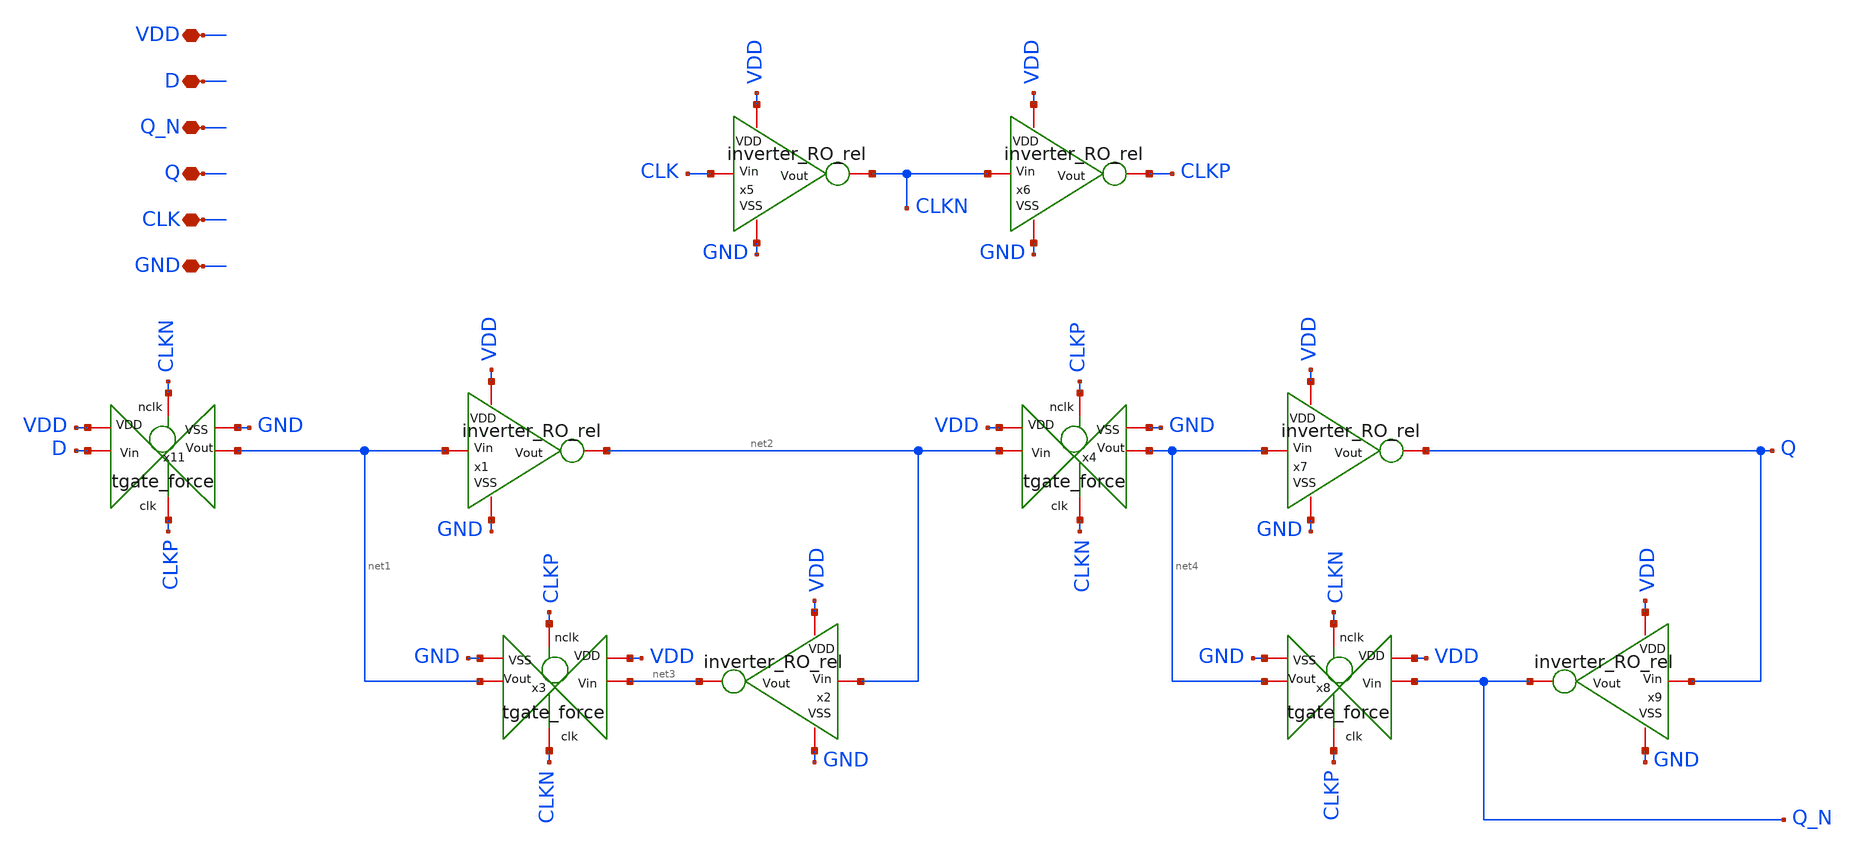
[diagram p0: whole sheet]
** sch_path: unic_cass_wrapper_user_project/ROs_reliability/FF.sch
**.subckt FF GND CLK VDD Q Q_N D
*.iopin GND
*.iopin CLK
*.iopin VDD
*.iopin Q
*.iopin Q_N
*.iopin D
x11 CLKN VDD D net1 GND CLKP tgate_force
x1 VDD net1 net2 GND inverter_RO_rel
x2 VDD net2 net3 GND inverter_RO_rel
x3 CLKP VDD net3 net1 GND CLKN tgate_force
x4 CLKP VDD net2 net4 GND CLKN tgate_force
x5 VDD CLK CLKN GND inverter_RO_rel
x6 VDD CLKN CLKP GND inverter_RO_rel
x7 VDD net4 Q GND inverter_RO_rel
x8 CLKN VDD Q_N net4 GND CLKP tgate_force
x9 VDD Q Q_N GND inverter_RO_rel
**.ends

* expanding   symbol:  tgate_force.sym # of pins=6
** sym_path: tgate_force.sym
** sch_path: tgate_force.sch
.subckt tgate_force nclk VDD Vin Vout VSS clk
*.iopin nclk
*.iopin clk
*.iopin VDD
*.iopin VSS
*.iopin Vout
*.iopin Vin
XM3 Vout nclk Vin VDD sg13_lv_pmos w=3.4u l=0.45u ng=1 m=4 mm_ok=1
XM4 Vout clk Vin VSS sg13_lv_nmos w=1.3u l=0.45u ng=1 m=4 mm_ok=1
.ends


* expanding   symbol:  inverter_RO_rel.sym # of pins=4
** sym_path: inverter_RO_rel.sym
** sch_path: inverter_RO_rel.sch
.subckt inverter_RO_rel VDD Vin Vout VSS
*.iopin VDD
*.iopin VSS
*.iopin Vin
*.iopin Vout
XM3 Vout Vin VDD VDD sg13_lv_pmos w=3.4u l=0.45u ng=1 m=4 mm_ok=1
XM1 VSS Vin Vout VSS sg13_lv_nmos w=1.3u l=0.45u ng=1 m=4 mm_ok=1
.ends

.end
